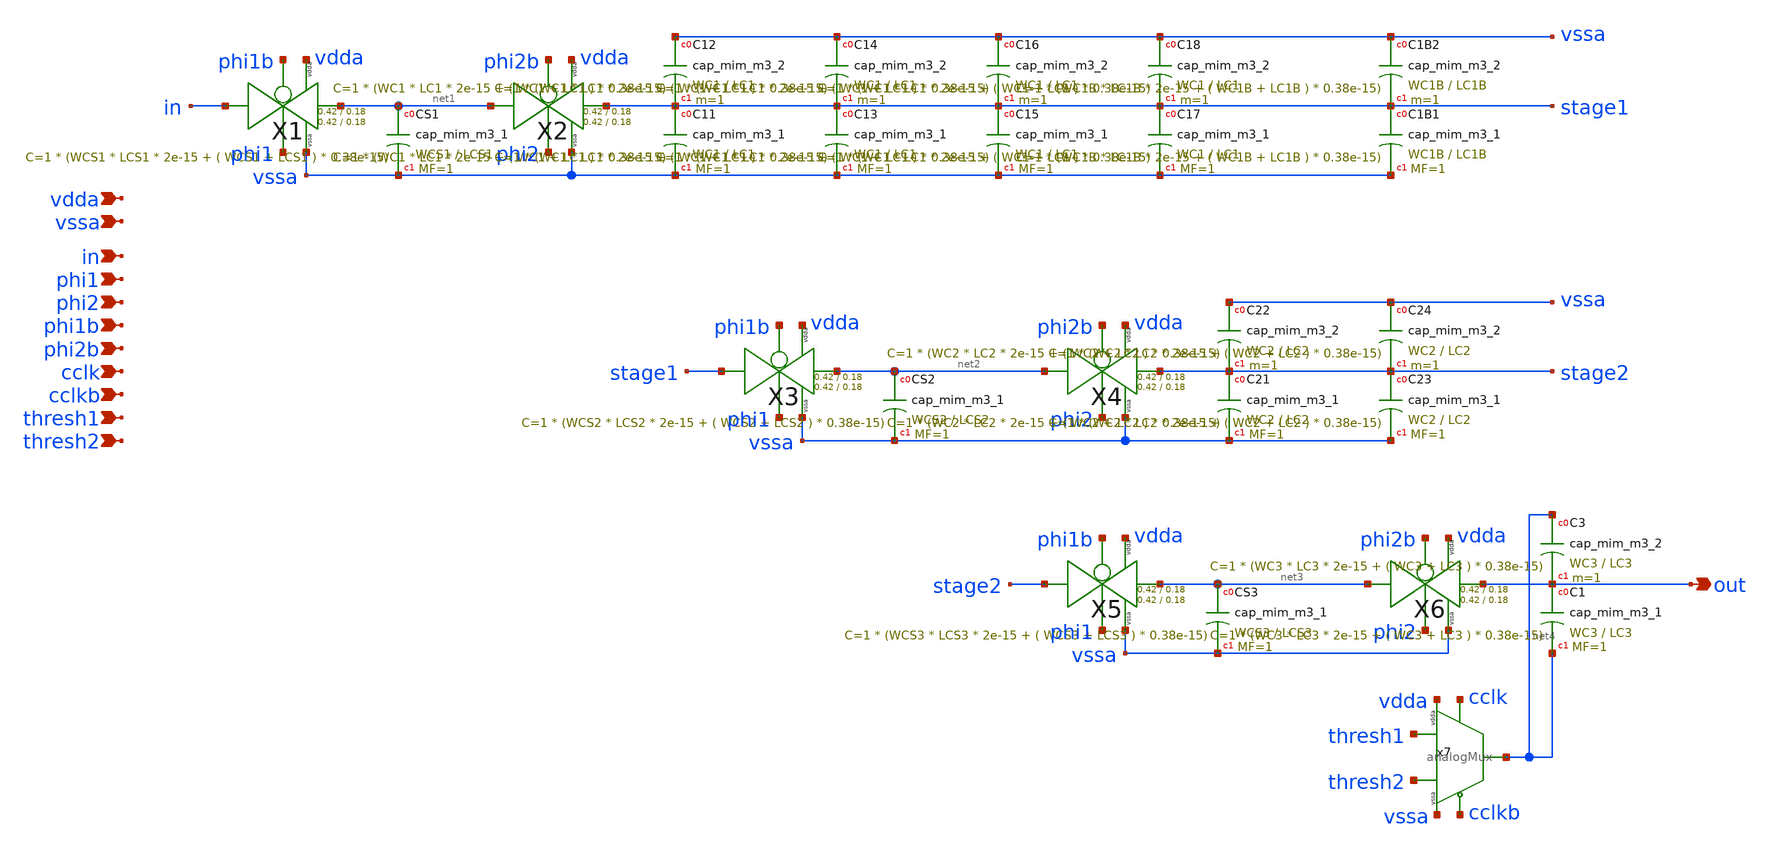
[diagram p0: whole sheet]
** sch_path: xschem/Switched_Caps/filter.sch
**.subckt filter in out phi1 phi2 phi1b phi2b cclk cclkb thresh1 thresh2 vdda vssa
*.ipin in
*.opin out
*.ipin phi1
*.ipin phi2
*.ipin phi1b
*.ipin phi2b
*.ipin cclk
*.ipin cclkb
*.ipin thresh1
*.ipin thresh2
*.ipin vdda
*.ipin vssa
XC12 vssa stage1 sky130_fd_pr__cap_mim_m3_2 W=WC1 L=LC1 MF=1 m=1
XCS1 net1 vssa sky130_fd_pr__cap_mim_m3_1 W=WCS1 L=LCS1 MF=1 m=1
XC11 stage1 vssa sky130_fd_pr__cap_mim_m3_1 W=WC1 L=LC1 MF=1 m=1
XCS2 net2 vssa sky130_fd_pr__cap_mim_m3_1 W=WCS2 L=LCS2 MF=1 m=1
XC3 net4 out sky130_fd_pr__cap_mim_m3_2 W=WC3 L=LC3 MF=1 m=1
XCS3 net3 vssa sky130_fd_pr__cap_mim_m3_1 W=WCS3 L=LCS3 MF=1 m=1
XC14 vssa stage1 sky130_fd_pr__cap_mim_m3_2 W=WC1 L=LC1 MF=1 m=1
XC13 stage1 vssa sky130_fd_pr__cap_mim_m3_1 W=WC1 L=LC1 MF=1 m=1
XC16 vssa stage1 sky130_fd_pr__cap_mim_m3_2 W=WC1 L=LC1 MF=1 m=1
XC15 stage1 vssa sky130_fd_pr__cap_mim_m3_1 W=WC1 L=LC1 MF=1 m=1
XC18 vssa stage1 sky130_fd_pr__cap_mim_m3_2 W=WC1 L=LC1 MF=1 m=1
XC17 stage1 vssa sky130_fd_pr__cap_mim_m3_1 W=WC1 L=LC1 MF=1 m=1
XC22 vssa stage2 sky130_fd_pr__cap_mim_m3_2 W=WC2 L=LC2 MF=1 m=1
XC21 stage2 vssa sky130_fd_pr__cap_mim_m3_1 W=WC2 L=LC2 MF=1 m=1
XC24 vssa stage2 sky130_fd_pr__cap_mim_m3_2 W=WC2 L=LC2 MF=1 m=1
XC23 stage2 vssa sky130_fd_pr__cap_mim_m3_1 W=WC2 L=LC2 MF=1 m=1
XC1B2 vssa stage1 sky130_fd_pr__cap_mim_m3_2 W=WC1B L=LC1B MF=1 m=1
XC1B1 stage1 vssa sky130_fd_pr__cap_mim_m3_1 W=WC1B L=LC1B MF=1 m=1
XC1 out net4 sky130_fd_pr__cap_mim_m3_1 W=WC3 L=LC3 MF=1 m=1
x7 thresh2 thresh1 cclk cclkb net4 vssa vdda analogMux
X1 in net1 phi1b phi1 vdda vssa transmission_gate Wpmos=0.42 Lpmos=0.18 Wnmos=0.42 Lnmos=0.18
X2 net1 stage1 phi2b phi2 vdda vssa transmission_gate Wpmos=0.42 Lpmos=0.18 Wnmos=0.42 Lnmos=0.18
X3 stage1 net2 phi1b phi1 vdda vssa transmission_gate Wpmos=0.42 Lpmos=0.18 Wnmos=0.42 Lnmos=0.18
X4 net2 stage2 phi2b phi2 vdda vssa transmission_gate Wpmos=0.42 Lpmos=0.18 Wnmos=0.42 Lnmos=0.18
X5 stage2 net3 phi1b phi1 vdda vssa transmission_gate Wpmos=0.42 Lpmos=0.18 Wnmos=0.42 Lnmos=0.18
X6 net3 out phi2b phi2 vdda vssa transmission_gate Wpmos=0.42 Lpmos=0.18 Wnmos=0.42 Lnmos=0.18
**.ends

* expanding   symbol:  mux/analogMux.sym # of pins=7
** sym_path: xschem/mux/analogMux.sym
** sch_path: xschem/mux/analogMux.sch
.subckt analogMux vref2 vref1 c cbar out vssa vdda
*.ipin vref1
*.opin out
*.ipin vref2
*.ipin c
*.ipin cbar
*.ipin vssa
*.ipin vdda
XM2 vref1 c out vssa sky130_fd_pr__nfet_01v8 L=0.15 W=0.42 nf=1 ad='int((nf+1)/2) * W/nf * 0.29' as='int((nf+2)/2) * W/nf * 0.29'
+ pd='2*int((nf+1)/2) * (W/nf + 0.29)' ps='2*int((nf+2)/2) * (W/nf + 0.29)' nrd='0.29 / W' nrs='0.29 / W'
+ sa=0 sb=0 sd=0 mult=1 m=1
XM4 vref1 cbar out vdda sky130_fd_pr__pfet_01v8 L=0.15 W=0.42 nf=1 ad='int((nf+1)/2) * W/nf * 0.29' as='int((nf+2)/2) * W/nf * 0.29'
+ pd='2*int((nf+1)/2) * (W/nf + 0.29)' ps='2*int((nf+2)/2) * (W/nf + 0.29)' nrd='0.29 / W' nrs='0.29 / W'
+ sa=0 sb=0 sd=0 mult=1 m=1
XM7 out cbar vref2 vssa sky130_fd_pr__nfet_01v8 L=0.15 W=0.42 nf=1 ad='int((nf+1)/2) * W/nf * 0.29' as='int((nf+2)/2) * W/nf * 0.29'
+ pd='2*int((nf+1)/2) * (W/nf + 0.29)' ps='2*int((nf+2)/2) * (W/nf + 0.29)' nrd='0.29 / W' nrs='0.29 / W'
+ sa=0 sb=0 sd=0 mult=1 m=1
XM8 out c vref2 vdda sky130_fd_pr__pfet_01v8 L=0.15 W=0.42 nf=1 ad='int((nf+1)/2) * W/nf * 0.29' as='int((nf+2)/2) * W/nf * 0.29'
+ pd='2*int((nf+1)/2) * (W/nf + 0.29)' ps='2*int((nf+2)/2) * (W/nf + 0.29)' nrd='0.29 / W' nrs='0.29 / W'
+ sa=0 sb=0 sd=0 mult=1 m=1
.ends


* expanding   symbol:  transmission_gate/transmission_gate.sym # of pins=6
** sym_path: xschem/transmission_gate/transmission_gate.sym
** sch_path: xschem/transmission_gate/transmission_gate.sch
.subckt transmission_gate in out ctrl_ ctrl vdda vssa  Wpmos=Wpmos Lpmos=Lpmos Wnmos=Wnmos
+ Lnmos=Lnmos
*.iopin in
*.iopin out
*.ipin ctrl_
*.ipin ctrl
*.ipin vdda
*.ipin vssa
XM1 out ctrl in vssa sky130_fd_pr__nfet_01v8 L=Lnmos W=Wnmos nf=1 ad='int((nf+1)/2) * W/nf * 0.29' as='int((nf+2)/2) * W/nf * 0.29'
+ pd='2*int((nf+1)/2) * (W/nf + 0.29)' ps='2*int((nf+2)/2) * (W/nf + 0.29)' nrd='0.29 / W' nrs='0.29 / W'
+ sa=0 sb=0 sd=0 mult=1 m=1
XM2 out ctrl_ in vdda sky130_fd_pr__pfet_01v8 L=Lpmos W=Wpmos nf=1 ad='int((nf+1)/2) * W/nf * 0.29' as='int((nf+2)/2) * W/nf * 0.29'
+ pd='2*int((nf+1)/2) * (W/nf + 0.29)' ps='2*int((nf+2)/2) * (W/nf + 0.29)' nrd='0.29 / W' nrs='0.29 / W'
+ sa=0 sb=0 sd=0 mult=1 m=1
.ends

.end
